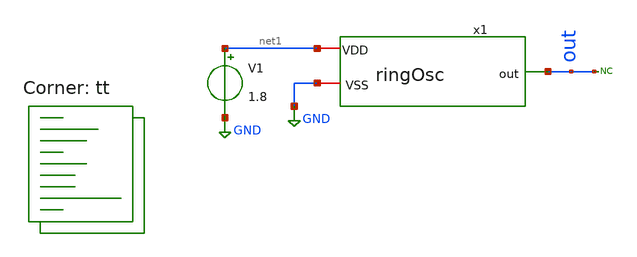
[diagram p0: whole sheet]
** sch_path: xsch/tb/ringOsc/ringOsc_tb_corners.sch
**.subckt ringOsc_tb_corners
x1 net1 GND out ringOsc
* noconn out
V1 net1 GND 1.8
**** begin user architecture code



.control
set temp=27
tran 0.1p 10n
wrdata ringOsc_tran_corners.csv v(out)
.endc


.lib $::SKYWATER_MODELS/sky130.lib.spice tt
**** end user architecture code
**.ends

* expanding   symbol:  ip/ringOsc/ringOsc.sym # of pins=3
** sym_path: ip/ringOsc/ringOsc.sym
** sch_path: ip/ringOsc/ringOsc.sch
.subckt ringOsc VDD VSS out
*.opin out
*.iopin VDD
*.iopin VSS
x1 VDD out net1 VSS inv
x2 VDD net1 net2 VSS inv
x3 VDD net2 out VSS inv
.ends


* expanding   symbol:  ip/inv/inv.sym # of pins=4
** sym_path: xsch/ip/inv/inv.sym
** sch_path: xsch/ip/inv/inv.sch
.subckt inv VDD in out VSS
*.ipin in
*.opin out
*.iopin VDD
*.iopin VSS
XMN out in VSS VSS sky130_fd_pr__nfet_01v8 L=0.15 W=1 nf=1 ad='int((1 + 1)/2) * 1 / 1 * 0.29' as='int((1 + 2)/2) * 1 / 1 * 0.29'
+ pd='2*int((1 + 1)/2) * (1 / 1 + 0.29)' ps='2*int((1 + 2)/2) * (1 / 1 + 0.29)' nrd='0.29 / 1 ' nrs='0.29 / 1 '
+ sa=0 sb=0 sd=0 mult=1 m=1
XMP out in VDD VDD sky130_fd_pr__pfet_01v8 L=0.15 W=2 nf=1 ad='int((nf+1)/2) * W/nf * 0.29' as='int((nf+2)/2) * W/nf * 0.29'
+ pd='2*int((nf+1)/2) * (W/nf + 0.29)' ps='2*int((nf+2)/2) * (W/nf + 0.29)' nrd='0.29 / W' nrs='0.29 / W'
+ sa=0 sb=0 sd=0 mult=1 m=1
.ends

.GLOBAL GND
.end
